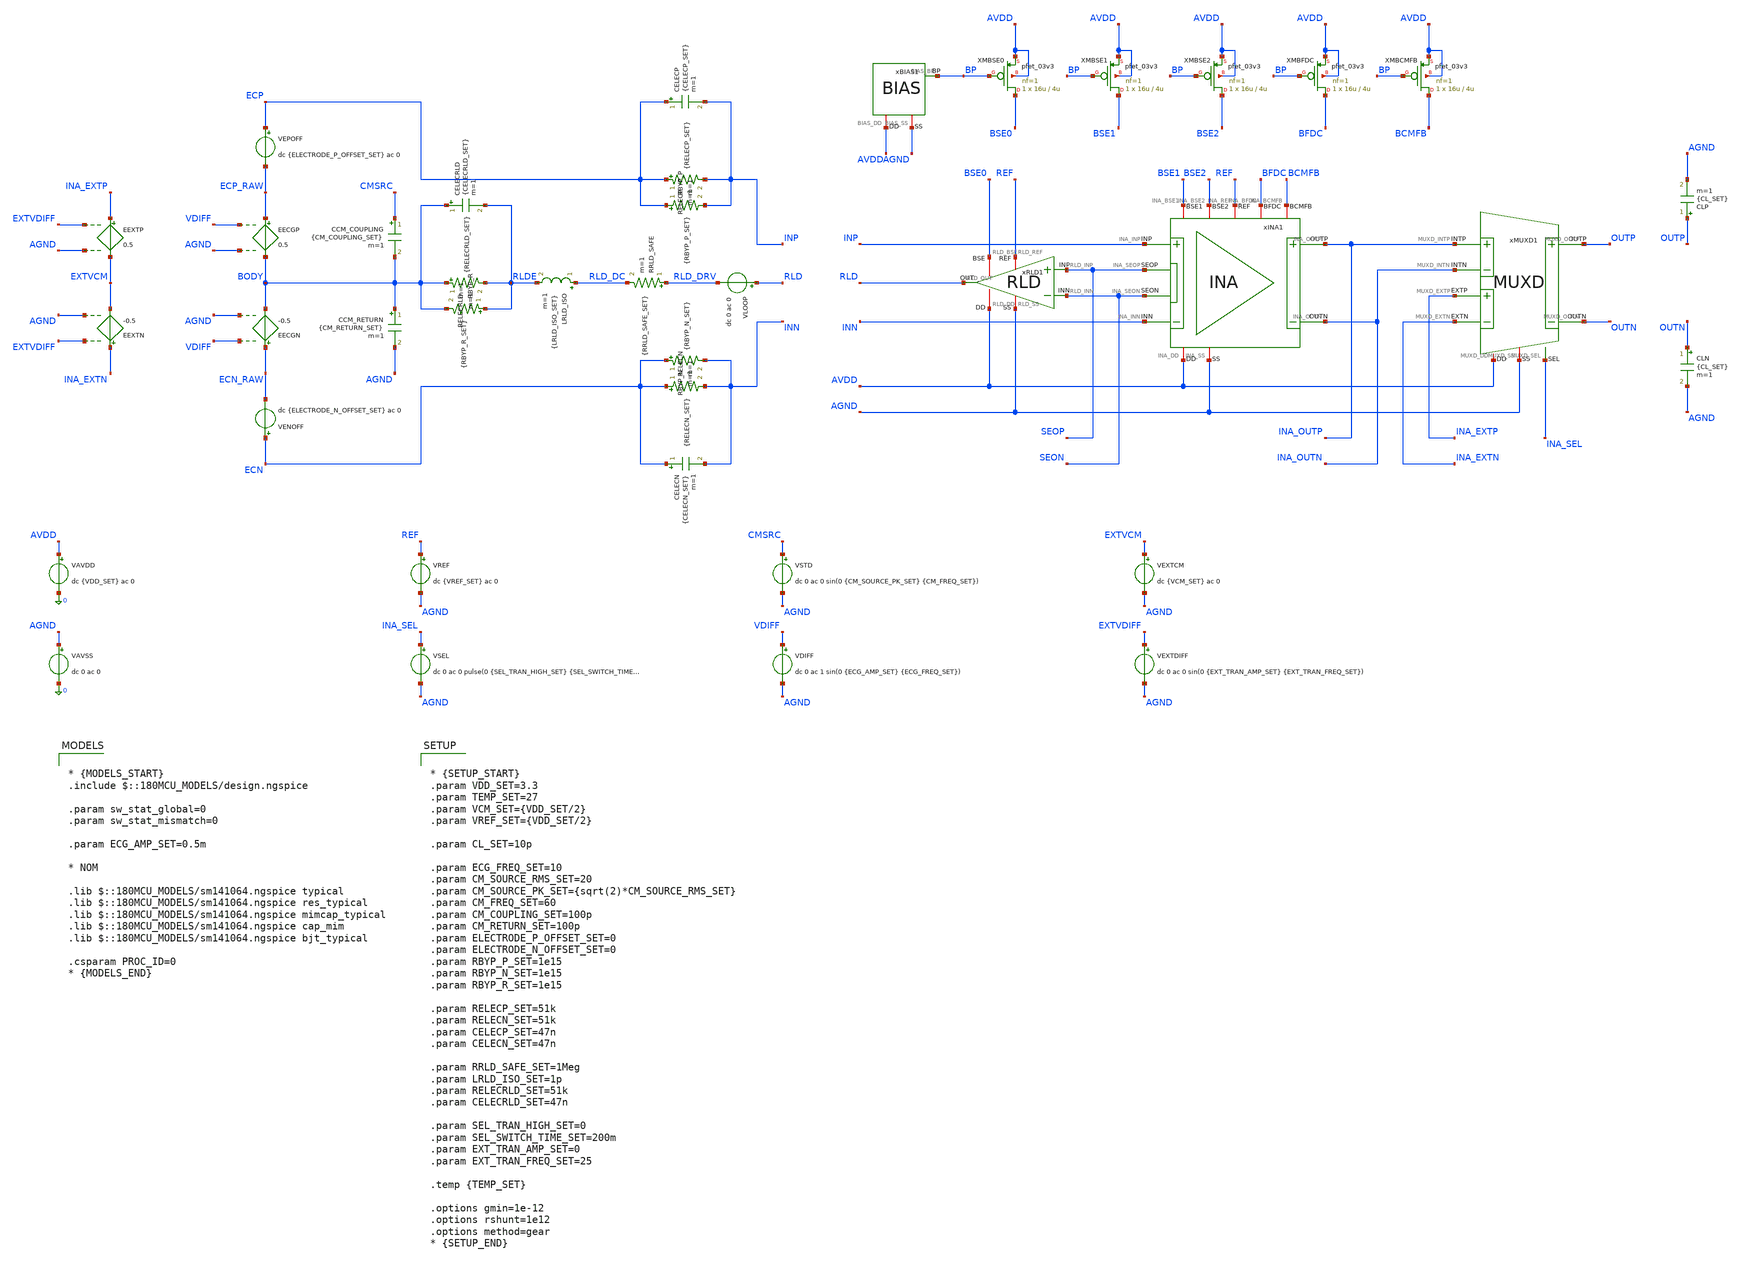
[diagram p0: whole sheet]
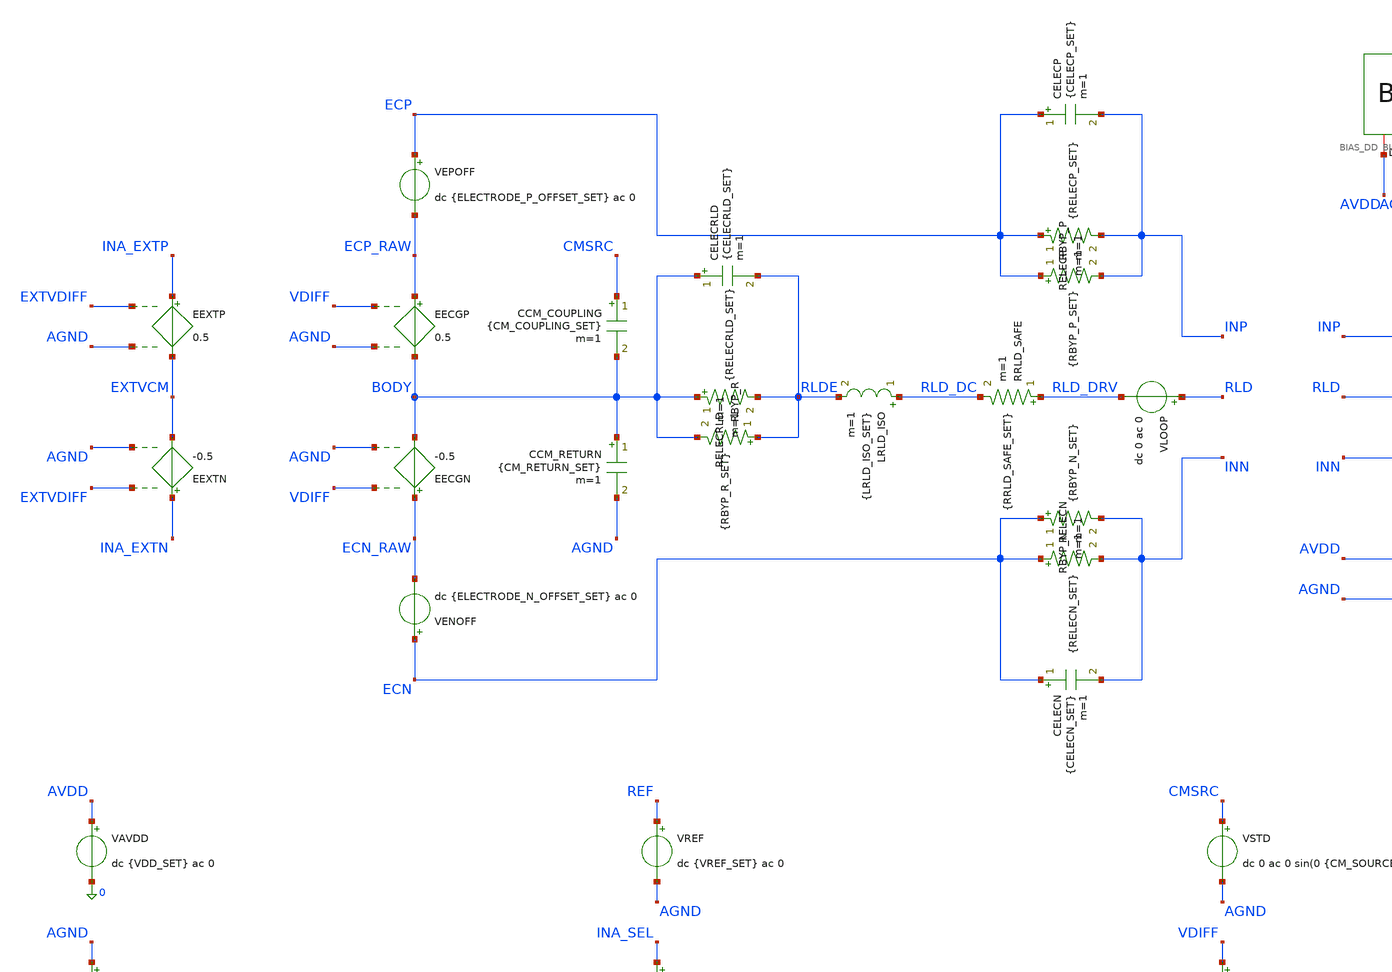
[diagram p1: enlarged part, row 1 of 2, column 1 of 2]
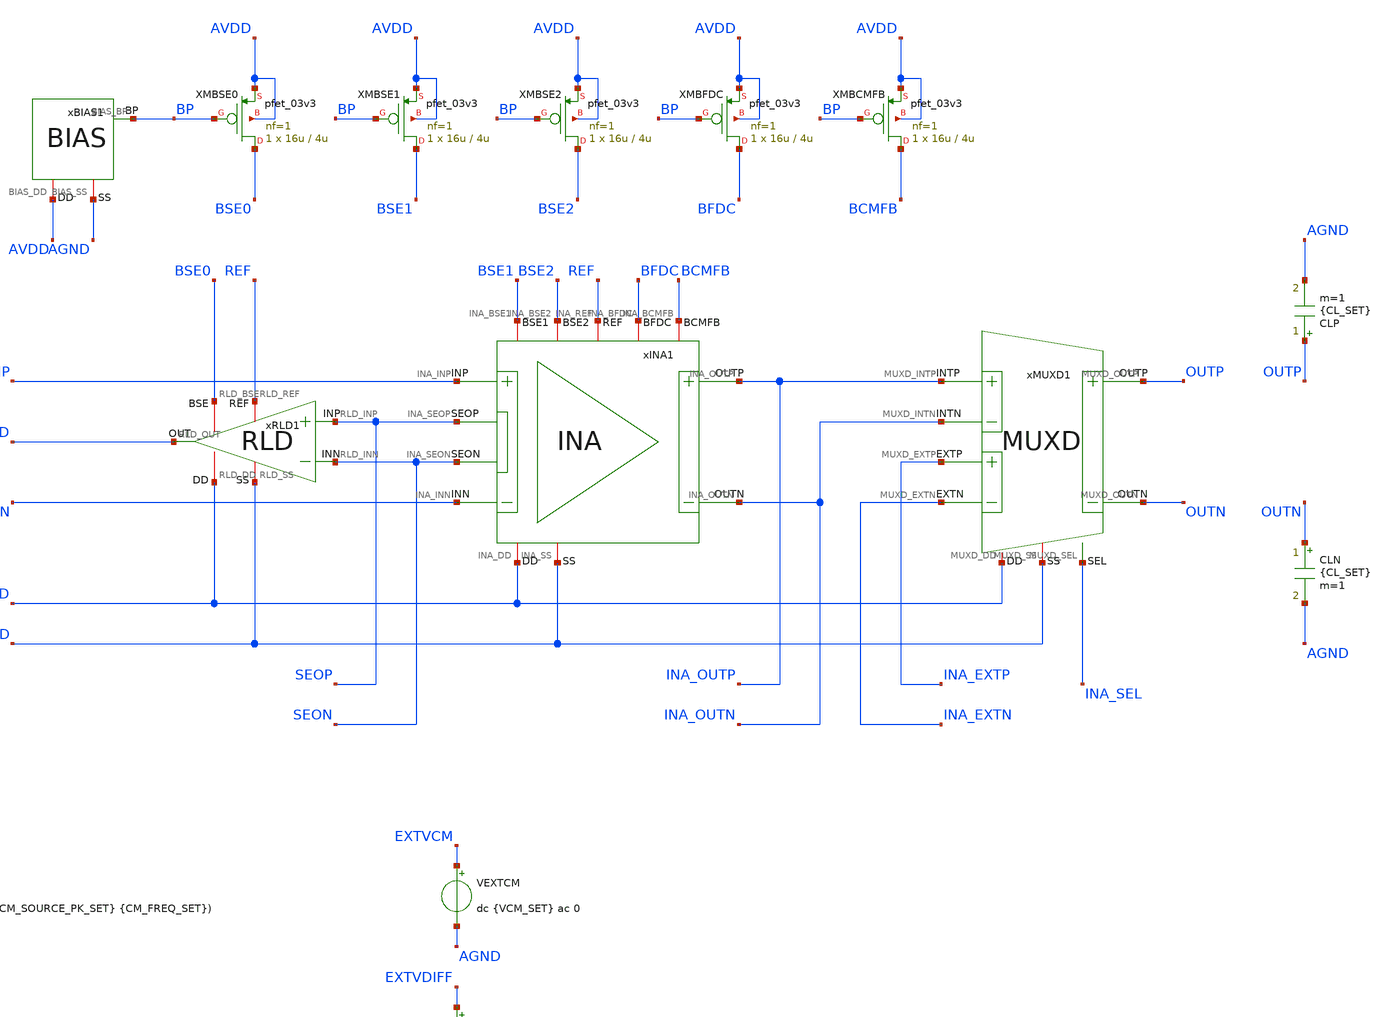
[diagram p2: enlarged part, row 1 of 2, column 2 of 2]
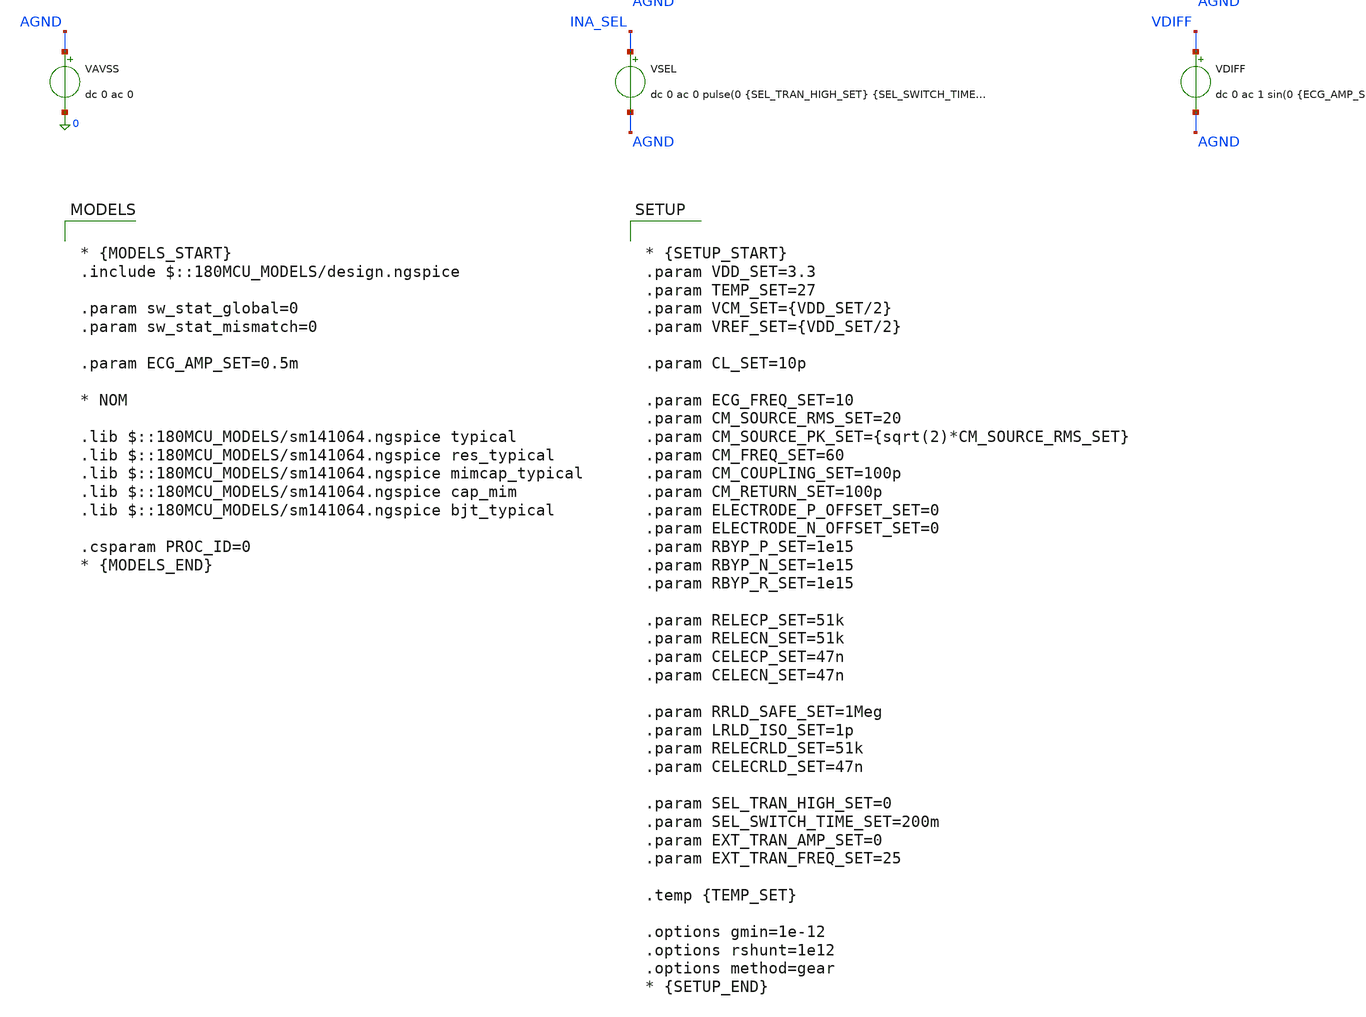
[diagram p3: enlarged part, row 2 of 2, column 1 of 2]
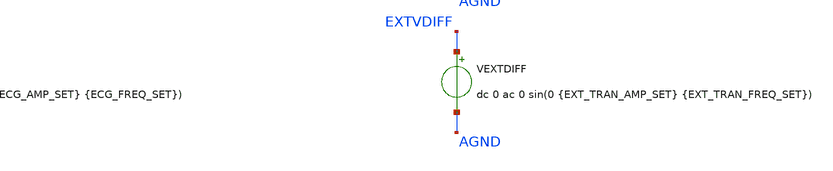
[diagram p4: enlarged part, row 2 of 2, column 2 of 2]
** sch_path: Design_Files/IC Design/Testbench/AFE_BLOCKS/INA_RLD/INA_RLD_TB_PVT_NOM.sch
**.subckt INA_RLD_TB_PVT_NOM
xMUXD1 AVDD AGND INA_OUTP INA_OUTN OUTN OUTP INA_EXTP INA_EXTN INA_SEL MUXD
xINA1 AVDD AGND INP INN INA_OUTN BFDC INA_OUTP BCMFB REF SEON SEOP BSE1 BSE2 INA
xRLD1 AVDD AGND SEOP SEON RLD REF BSE0 RLD
CLP OUTP AGND {CL_SET} m=1
CLN OUTN AGND {CL_SET} m=1
xBIAS1 AVDD AGND BP BIAS
XMBSE0 BSE0 BP AVDD AVDD pfet_03v3 L=4u W=16u nf=1 ad='int((nf+1)/2) * W/nf * 0.18u' as='int((nf+2)/2) * W/nf * 0.18u'
+ pd='2*int((nf+1)/2) * (W/nf + 0.18u)' ps='2*int((nf+2)/2) * (W/nf + 0.18u)' nrd='0.18u / W' nrs='0.18u / W'
+ sa=0 sb=0 sd=0 m=1
XMBSE1 BSE1 BP AVDD AVDD pfet_03v3 L=4u W=16u nf=1 ad='int((nf+1)/2) * W/nf * 0.18u' as='int((nf+2)/2) * W/nf * 0.18u'
+ pd='2*int((nf+1)/2) * (W/nf + 0.18u)' ps='2*int((nf+2)/2) * (W/nf + 0.18u)' nrd='0.18u / W' nrs='0.18u / W'
+ sa=0 sb=0 sd=0 m=1
XMBSE2 BSE2 BP AVDD AVDD pfet_03v3 L=4u W=16u nf=1 ad='int((nf+1)/2) * W/nf * 0.18u' as='int((nf+2)/2) * W/nf * 0.18u'
+ pd='2*int((nf+1)/2) * (W/nf + 0.18u)' ps='2*int((nf+2)/2) * (W/nf + 0.18u)' nrd='0.18u / W' nrs='0.18u / W'
+ sa=0 sb=0 sd=0 m=1
XMBFDC BFDC BP AVDD AVDD pfet_03v3 L=4u W=16u nf=1 ad='int((nf+1)/2) * W/nf * 0.18u' as='int((nf+2)/2) * W/nf * 0.18u'
+ pd='2*int((nf+1)/2) * (W/nf + 0.18u)' ps='2*int((nf+2)/2) * (W/nf + 0.18u)' nrd='0.18u / W' nrs='0.18u / W'
+ sa=0 sb=0 sd=0 m=1
XMBCMFB BCMFB BP AVDD AVDD pfet_03v3 L=4u W=16u nf=1 ad='int((nf+1)/2) * W/nf * 0.18u' as='int((nf+2)/2) * W/nf * 0.18u'
+ pd='2*int((nf+1)/2) * (W/nf + 0.18u)' ps='2*int((nf+2)/2) * (W/nf + 0.18u)' nrd='0.18u / W' nrs='0.18u / W'
+ sa=0 sb=0 sd=0 m=1
VAVDD AVDD 0 dc {VDD_SET} ac 0
.save i(vavdd)
VAVSS AGND 0 dc 0 ac 0
VSTD CMSRC AGND dc 0 ac 0 sin(0 {CM_SOURCE_PK_SET} {CM_FREQ_SET})
EECGP ECP_RAW BODY VDIFF AGND 0.5
EECGN ECN_RAW BODY VDIFF AGND -0.5
EEXTP INA_EXTP EXTVCM EXTVDIFF AGND 0.5
VDIFF VDIFF AGND dc 0 ac 1 sin(0 {ECG_AMP_SET} {ECG_FREQ_SET})
VLOOP RLD RLD_DRV dc 0 ac 0
.save i(vloop)
VSEL INA_SEL AGND dc 0 ac 0 pulse(0 {SEL_TRAN_HIGH_SET} {SEL_SWITCH_TIME_SET} 1u 1u 400m 800m)
VEXTCM EXTVCM AGND dc {VCM_SET} ac 0
VEXTDIFF EXTVDIFF AGND dc 0 ac 0 sin(0 {EXT_TRAN_AMP_SET} {EXT_TRAN_FREQ_SET})
EEXTN INA_EXTN EXTVCM EXTVDIFF AGND -0.5
CCM_COUPLING CMSRC BODY {CM_COUPLING_SET} m=1
RELECP ECP INP {RELECP_SET} m=1
RELECN ECN INN {RELECN_SET} m=1
CELECP ECP INP {CELECP_SET} m=1
CELECN ECN INN {CELECN_SET} m=1
RRLD_SAFE RLD_DRV RLD_DC {RRLD_SAFE_SET} m=1
RELECRLD BODY RLDE {RELECRLD_SET} m=1
CELECRLD BODY RLDE {CELECRLD_SET} m=1
VEPOFF ECP ECP_RAW dc {ELECTRODE_P_OFFSET_SET} ac 0
VENOFF ECN ECN_RAW dc {ELECTRODE_N_OFFSET_SET} ac 0
CCM_RETURN BODY AGND {CM_RETURN_SET} m=1
RBYP_P ECP INP {RBYP_P_SET} m=1
RBYP_N ECN INN {RBYP_N_SET} m=1
RBYP_R RLDE BODY {RBYP_R_SET} m=1
LRLD_ISO RLD_DC RLDE {LRLD_ISO_SET} m=1
VREF REF AGND dc {VREF_SET} ac 0
.save i(vref)
**** begin user architecture code

* {MODELS_START}
.include $::180MCU_MODELS/design.ngspice

.param sw_stat_global=0
.param sw_stat_mismatch=0

.param ECG_AMP_SET=0.5m

* NOM

.lib $::180MCU_MODELS/sm141064.ngspice typical
.lib $::180MCU_MODELS/sm141064.ngspice res_typical
.lib $::180MCU_MODELS/sm141064.ngspice mimcap_typical
.lib $::180MCU_MODELS/sm141064.ngspice cap_mim
.lib $::180MCU_MODELS/sm141064.ngspice bjt_typical

.csparam PROC_ID=0
* {MODELS_END}



* {SETUP_START}
.param VDD_SET=3.3
.param TEMP_SET=27
.param VCM_SET={VDD_SET/2}
.param VREF_SET={VDD_SET/2}

.param CL_SET=10p

.param ECG_FREQ_SET=10
.param CM_SOURCE_RMS_SET=20
.param CM_SOURCE_PK_SET={sqrt(2)*CM_SOURCE_RMS_SET}
.param CM_FREQ_SET=60
.param CM_COUPLING_SET=100p
.param CM_RETURN_SET=100p
.param ELECTRODE_P_OFFSET_SET=0
.param ELECTRODE_N_OFFSET_SET=0
.param RBYP_P_SET=1e15
.param RBYP_N_SET=1e15
.param RBYP_R_SET=1e15

.param RELECP_SET=51k
.param RELECN_SET=51k
.param CELECP_SET=47n
.param CELECN_SET=47n

.param RRLD_SAFE_SET=1Meg
.param LRLD_ISO_SET=1p
.param RELECRLD_SET=51k
.param CELECRLD_SET=47n

.param SEL_TRAN_HIGH_SET=0
.param SEL_SWITCH_TIME_SET=200m
.param EXT_TRAN_AMP_SET=0
.param EXT_TRAN_FREQ_SET=25

.temp {TEMP_SET}

.options gmin=1e-12
.options rshunt=1e12
.options method=gear
* {SETUP_END}




* {MEAS_START}
.control

destroy all

set noaskquit
set wr_singlescale
unset wr_vecnames

option klu
option numdgt=15
option method=gear
option maxord=2
option plotwinsize=0

if $&PROC_ID = 0
set proc=NOM
else
if $&PROC_ID = 1
set proc=FF
else
if $&PROC_ID = 2
set proc=SS
else
if $&PROC_ID = 3
set proc=FS
else
set proc=SF
end
end
end
end

shell mkdir -p /foss/designs/ECG_Acquisition_IC/Measurement_Results/IC_Simulation/AFE_BLOCKS/INA_RLD/{$proc}.Result_txt
shell rm -f /foss/designs/ECG_Acquisition_IC/Measurement_Results/IC_Simulation/AFE_BLOCKS/INA_RLD/{$proc}.Result_txt/{$proc}.*.txt

foreach vddval 3.3 3.0 3.6
foreach tval 27 -40 125

if $vddval = 3.3
if $tval = 27
set env=nom
else
if $tval = -40
set env=tl
else
set env=th
end
end
else
if $vddval = 3.0
if $tval = 27
set env=vl
else
if $tval = -40
set env=vltl
else
set env=vlth
end
end
else
if $tval = 27
set env=vh
else
if $tval = -40
set env=vhtl
else
set env=vhth
end
end
end
end

alterparam VDD_SET=$vddval
alterparam TEMP_SET=$tval

reset

save all
save @m.xmbse0.m0[id]
save @m.xmbse1.m0[id]
save @m.xmbse2.m0[id]
save @m.xmbfdc.m0[id]
save @m.xmbcmfb.m0[id]

foreach emode 0

* NOMINAL ELECTRODE MODEL
set elec=bal
alter RELECP 51k
alter RELECN 51k
alter CELECP 47n
alter CELECN 47n
alter RELECRLD 51k
alter CELECRLD 47n
alter RBYP_P 1e15
alter RBYP_N 1e15
alter RBYP_R 1e15


* OFFSET

alter RRLD_SAFE 1Meg
alter @VSEL[DC]=0
alter @VDIFF[DC]=0

alter @VDIFF[ACMAG]=0
alter @VSTD[ACMAG]=0
alter @VLOOP[ACMAG]=0
alter @VEXTDIFF[ACMAG]=0
alter @VREF[ACMAG]=0
alter @VAVDD[ACMAG]=0
alter @VAVSS[ACMAG]=0

dc VDIFF -3m 3m 50u

let ina_out_diff=v(INA_OUTP)-v(INA_OUTN)

meas dc vos_meas when ina_out_diff=0 cross=1

set vos_val=$&vos_meas

echo $vos_val > /foss/designs/ECG_Acquisition_IC/Measurement_Results/IC_Simulation/AFE_BLOCKS/INA_RLD/{$proc}.Result_txt/{$proc}.vos_{$env}_{$elec}.txt

destroy all

alter @VDIFF[DC]=$vos_val


* OP

alter RRLD_SAFE 1Meg
alter @VSEL[DC]=0

alter @VDIFF[ACMAG]=0
alter @VSTD[ACMAG]=0
alter @VLOOP[ACMAG]=0
alter @VEXTDIFF[ACMAG]=0
alter @VREF[ACMAG]=0
alter @VAVDD[ACMAG]=0
alter @VAVSS[ACMAG]=0

op

let vin_cm=0.5*(v(INP)+v(INN))-v(AGND)
let vin_diff=v(INP)-v(INN)
let se_cm=0.5*(v(SEOP)+v(SEON))-v(AGND)
let se_diff=v(SEOP)-v(SEON)
let ina_out_cm=0.5*(v(INA_OUTP)+v(INA_OUTN))-v(AGND)
let ina_out_diff=v(INA_OUTP)-v(INA_OUTN)
let out_cm=0.5*(v(OUTP)+v(OUTN))-v(AGND)
let out_diff=v(OUTP)-v(OUTN)

let idd_total=abs(vavdd#branch)
let power_total=(v(AVDD)-v(AGND))*idd_total
let irld=abs(vloop#branch)

let ibse0=abs(@m.xmbse0.m0[id])
let ibse1=abs(@m.xmbse1.m0[id])
let ibse2=abs(@m.xmbse2.m0[id])
let ibfdc=abs(@m.xmbfdc.m0[id])
let ibcmfb=abs(@m.xmbcmfb.m0[id])

wrdata /foss/designs/ECG_Acquisition_IC/Measurement_Results/IC_Simulation/AFE_BLOCKS/INA_RLD/{$proc}.Result_txt/{$proc}.op_{$env}_{$elec}.txt
+ v(AVDD) v(REF) v(BP) vin_cm vin_diff v(SEOP) v(SEON) se_cm se_diff v(INA_OUTP) v(INA_OUTN) ina_out_cm
+ ina_out_diff v(OUTP) v(OUTN) out_cm out_diff v(RLD) v(BODY) irld idd_total power_total ibse0 ibse1 ibse2
+ ibfdc ibcmfb

destroy all


* INA AC

alter RRLD_SAFE 1Meg
alter @VSEL[DC]=0

alter @VDIFF[ACMAG]=1
alter @VDIFF[ACPHASE]=0
alter @VSTD[ACMAG]=0
alter @VLOOP[ACMAG]=0
alter @VEXTDIFF[ACMAG]=0
alter @VREF[ACMAG]=0
alter @VAVDD[ACMAG]=0
alter @VAVSS[ACMAG]=0

ac dec 50 0.01 10Meg

let vin_diff=v(INP)-v(INN)
let se_diff=v(SEOP)-v(SEON)
let ina_out_diff=v(INA_OUTP)-v(INA_OUTN)
let out_diff=v(OUTP)-v(OUTN)

let vin_diff_real=real(vin_diff)
let vin_diff_imag=imag(vin_diff)

let se_diff_real=real(se_diff)
let se_diff_imag=imag(se_diff)

let ina_out_diff_real=real(ina_out_diff)
let ina_out_diff_imag=imag(ina_out_diff)

let out_diff_real=real(out_diff)
let out_diff_imag=imag(out_diff)

let rld_real=real(v(RLD))
let rld_imag=imag(v(RLD))

setscale frequency

wrdata /foss/designs/ECG_Acquisition_IC/Measurement_Results/IC_Simulation/AFE_BLOCKS/INA_RLD/{$proc}.Result_txt/{$proc}.diff_ac_{$env}_{$elec}.txt
+ vin_diff_real vin_diff_imag se_diff_real se_diff_imag ina_out_diff_real ina_out_diff_imag out_diff_real
+ out_diff_imag rld_real rld_imag

destroy all


* RLD OFF

* Keep the DC bias; isolate the RLD path in AC.
alter RRLD_SAFE 1Meg
alter LRLD_ISO 1e12
alter @VSEL[DC]=0

alter @VDIFF[ACMAG]=0
alter @VSTD[ACMAG]=1
alter @VSTD[ACPHASE]=0
alter @VLOOP[ACMAG]=0
alter @VEXTDIFF[ACMAG]=0
alter @VREF[ACMAG]=0
alter @VAVDD[ACMAG]=0
alter @VAVSS[ACMAG]=0

op

let rld_off_vin_cm=0.5*(v(INP)+v(INN))-v(AGND)
let rld_off_body=v(BODY)-v(AGND)

wrdata /foss/designs/ECG_Acquisition_IC/Measurement_Results/IC_Simulation/AFE_BLOCKS/INA_RLD/{$proc}.Result_txt/{$proc}.rld_off_op_{$env}_{$elec}.txt
+ rld_off_vin_cm rld_off_body v(INP) v(INN)

destroy all

ac dec 50 0.01 100k

let vcm_src=v(CMSRC)-v(AGND)
let body=v(BODY)-v(AGND)
let vin_cm=0.5*(v(INP)+v(INN))-v(AGND)
let se_cm=0.5*(v(SEOP)+v(SEON))-v(AGND)
let ina_out_diff=v(INA_OUTP)-v(INA_OUTN)
let out_diff=v(OUTP)-v(OUTN)

let vcm_src_real=real(vcm_src)
let vcm_src_imag=imag(vcm_src)

let body_real=real(body)
let body_imag=imag(body)

let vin_cm_real=real(vin_cm)
let vin_cm_imag=imag(vin_cm)

let se_cm_real=real(se_cm)
let se_cm_imag=imag(se_cm)

let ina_out_diff_real=real(ina_out_diff)
let ina_out_diff_imag=imag(ina_out_diff)

let out_diff_real=real(out_diff)
let out_diff_imag=imag(out_diff)

let rld_real=real(v(RLD))
let rld_imag=imag(v(RLD))

setscale frequency

wrdata /foss/designs/ECG_Acquisition_IC/Measurement_Results/IC_Simulation/AFE_BLOCKS/INA_RLD/{$proc}.Result_txt/{$proc}.cm_off_ac_{$env}_{$elec}.txt
+ vcm_src_real vcm_src_imag body_real body_imag vin_cm_real vin_cm_imag se_cm_real se_cm_imag out_diff_real
+ out_diff_imag rld_real rld_imag

wrdata /foss/designs/ECG_Acquisition_IC/Measurement_Results/IC_Simulation/AFE_BLOCKS/INA_RLD/{$proc}.Result_txt/{$proc}.ina_cmrr_ac_{$env}_{$elec}.txt
+ vin_cm_real vin_cm_imag ina_out_diff_real ina_out_diff_imag

destroy all


* RLD ON

alter RRLD_SAFE 1Meg
alter LRLD_ISO 1p
alter @VSEL[DC]=0

alter @VDIFF[ACMAG]=0
alter @VSTD[ACMAG]=1
alter @VSTD[ACPHASE]=0
alter @VLOOP[ACMAG]=0
alter @VEXTDIFF[ACMAG]=0
alter @VREF[ACMAG]=0
alter @VAVDD[ACMAG]=0
alter @VAVSS[ACMAG]=0

ac dec 50 0.01 10k

let vcm_src=v(CMSRC)-v(AGND)
let body=v(BODY)-v(AGND)
let vin_cm=0.5*(v(INP)+v(INN))-v(AGND)
let se_cm=0.5*(v(SEOP)+v(SEON))-v(AGND)
let out_diff=v(OUTP)-v(OUTN)

let vcm_src_real=real(vcm_src)
let vcm_src_imag=imag(vcm_src)

let body_real=real(body)
let body_imag=imag(body)

let vin_cm_real=real(vin_cm)
let vin_cm_imag=imag(vin_cm)

let se_cm_real=real(se_cm)
let se_cm_imag=imag(se_cm)

let out_diff_real=real(out_diff)
let out_diff_imag=imag(out_diff)

let rld_real=real(v(RLD))
let rld_imag=imag(v(RLD))

setscale frequency

wrdata /foss/designs/ECG_Acquisition_IC/Measurement_Results/IC_Simulation/AFE_BLOCKS/INA_RLD/{$proc}.Result_txt/{$proc}.cm_on_ac_{$env}_{$elec}.txt
+ vcm_src_real vcm_src_imag body_real body_imag vin_cm_real vin_cm_imag se_cm_real se_cm_imag out_diff_real
+ out_diff_imag rld_real rld_imag

destroy all


* PSRR+

alter RRLD_SAFE 1Meg
alter @VSEL[DC]=0

alter @VDIFF[ACMAG]=0
alter @VSTD[ACMAG]=0
alter @VLOOP[ACMAG]=0
alter @VEXTDIFF[ACMAG]=0
alter @VREF[ACMAG]=0

alter @VAVDD[ACMAG]=1
alter @VAVDD[ACPHASE]=0
alter @VAVSS[ACMAG]=0

ac dec 50 0.01 100k

let vsup=v(AVDD)-v(AGND)
let ina_out_diff=v(INA_OUTP)-v(INA_OUTN)
let out_diff=v(OUTP)-v(OUTN)

let vsup_real=real(vsup)
let vsup_imag=imag(vsup)

let ina_out_diff_real=real(ina_out_diff)
let ina_out_diff_imag=imag(ina_out_diff)

let out_diff_real=real(out_diff)
let out_diff_imag=imag(out_diff)

setscale frequency

wrdata /foss/designs/ECG_Acquisition_IC/Measurement_Results/IC_Simulation/AFE_BLOCKS/INA_RLD/{$proc}.Result_txt/{$proc}.psrrp_ac_{$env}_{$elec}.txt
+ vsup_real vsup_imag ina_out_diff_real ina_out_diff_imag out_diff_real out_diff_imag

destroy all


* PSRR-

alter RRLD_SAFE 1Meg
alter @VSEL[DC]=0

alter @VDIFF[ACMAG]=0
alter @VSTD[ACMAG]=0
alter @VLOOP[ACMAG]=0
alter @VEXTDIFF[ACMAG]=0
alter @VREF[ACMAG]=0

alter @VAVDD[ACMAG]=0
alter @VAVSS[ACMAG]=1
alter @VAVSS[ACPHASE]=0

ac dec 50 0.01 100k

let vsup=v(AVDD)-v(AGND)
let ina_out_diff=v(INA_OUTP)-v(INA_OUTN)
let out_diff=v(OUTP)-v(OUTN)

let vsup_real=real(vsup)
let vsup_imag=imag(vsup)

let ina_out_diff_real=real(ina_out_diff)
let ina_out_diff_imag=imag(ina_out_diff)

let out_diff_real=real(out_diff)
let out_diff_imag=imag(out_diff)

setscale frequency

wrdata /foss/designs/ECG_Acquisition_IC/Measurement_Results/IC_Simulation/AFE_BLOCKS/INA_RLD/{$proc}.Result_txt/{$proc}.psrrn_ac_{$env}_{$elec}.txt
+ vsup_real vsup_imag ina_out_diff_real ina_out_diff_imag out_diff_real out_diff_imag

destroy all


* RLD LOOP

alter RRLD_SAFE 1Meg
alter LRLD_ISO 1p
alter @VSEL[DC]=0

alter @VDIFF[ACMAG]=0
alter @VSTD[ACMAG]=0
alter @VLOOP[ACMAG]=1
alter @VLOOP[ACPHASE]=0
alter @VEXTDIFF[ACMAG]=0
alter @VREF[ACMAG]=0
alter @VAVDD[ACMAG]=0
alter @VAVSS[ACMAG]=0

ac dec 50 0.01 100k

let loop_in=v(RLD_DRV)-v(AGND)
let loop_out=v(RLD)-v(AGND)
let body=v(BODY)-v(AGND)
let vin_cm=0.5*(v(INP)+v(INN))-v(AGND)
let se_cm=0.5*(v(SEOP)+v(SEON))-v(AGND)

let loop_in_real=real(loop_in)
let loop_in_imag=imag(loop_in)

let loop_out_real=real(loop_out)
let loop_out_imag=imag(loop_out)

let body_real=real(body)
let body_imag=imag(body)

let vin_cm_real=real(vin_cm)
let vin_cm_imag=imag(vin_cm)

let se_cm_real=real(se_cm)
let se_cm_imag=imag(se_cm)

setscale frequency

wrdata /foss/designs/ECG_Acquisition_IC/Measurement_Results/IC_Simulation/AFE_BLOCKS/INA_RLD/{$proc}.Result_txt/{$proc}.rld_loop_ac_{$env}_{$elec}.txt
+ loop_in_real loop_in_imag loop_out_real loop_out_imag body_real body_imag vin_cm_real vin_cm_imag se_cm_real
+ se_cm_imag

destroy all


* NOISE

alter RRLD_SAFE 1Meg
alter @VSEL[DC]=0

alter @VDIFF[ACMAG]=1
alter @VDIFF[ACPHASE]=0
alter @VSTD[ACMAG]=0
alter @VLOOP[ACMAG]=0
alter @VEXTDIFF[ACMAG]=0
alter @VREF[ACMAG]=0
alter @VAVDD[ACMAG]=0
alter @VAVSS[ACMAG]=0

option sparse

noise v(OUTP,OUTN) VDIFF dec 50 0.05 500

setplot previous
setscale frequency

wrdata /foss/designs/ECG_Acquisition_IC/Measurement_Results/IC_Simulation/AFE_BLOCKS/INA_RLD/{$proc}.Result_txt/{$proc}.noise_{$env}_{$elec}.txt
+ onoise_spectrum inoise_spectrum

destroy all


* INA VTC

* Balanced electrodes, RLD ON, internal INA path.
alter RELECP 51k
alter RELECN 51k
alter CELECP 47n
alter CELECN 47n
alter RELECRLD 51k
alter CELECRLD 47n
alter RBYP_P 1e15
alter RBYP_N 1e15
alter RBYP_R 1e15
alter RRLD_SAFE 1Meg
alter LRLD_ISO 1p
alter @VSEL[DC]=0

* No AC excitation.
alter @VDIFF[ACMAG]=0
alter @VSTD[ACMAG]=0
alter @VLOOP[ACMAG]=0
alter @VEXTDIFF[ACMAG]=0
alter @VREF[ACMAG]=0
alter @VAVDD[ACMAG]=0
alter @VAVSS[ACMAG]=0

* Sweep beyond the required ECG plus offset range.
dc VDIFF -20m 20m 50u

let vin_diff=v(INP)-v(INN)
let ina_outp=v(INA_OUTP)-v(AGND)
let ina_outn=v(INA_OUTN)-v(AGND)
let ina_out_cm=0.5*(v(INA_OUTP)+v(INA_OUTN))-v(AGND)
let ina_out_diff=v(INA_OUTP)-v(INA_OUTN)

wrdata /foss/designs/ECG_Acquisition_IC/Measurement_Results/IC_Simulation/AFE_BLOCKS/INA_RLD/{$proc}.Result_txt/{$proc}.vtc_{$env}_{$elec}.txt
+ vin_diff ina_outp ina_outn ina_out_cm ina_out_diff

destroy all


* THD AT 60 HZ

* 5 mVpp (2.5 mV peak) differential input at 60 Hz.
alterparam ECG_AMP_SET=2.5m
alterparam ECG_FREQ_SET=60
alterparam CM_SOURCE_RMS_SET=0
alterparam ELECTRODE_P_OFFSET_SET=0
alterparam ELECTRODE_N_OFFSET_SET=0

reset

save v(INP) v(INN)
save v(INA_OUTP) v(INA_OUTN)
save v(OUTP) v(OUTN)

* Balanced electrodes, RLD ON, internal INA path.
alter RELECP 51k
alter RELECN 51k
alter CELECP 47n
alter CELECN 47n
alter RELECRLD 51k
alter CELECRLD 47n
alter RBYP_P 1e15
alter RBYP_N 1e15
alter RBYP_R 1e15
alter RRLD_SAFE 1Meg
alter LRLD_ISO 1p
alter @VSEL[DC]=0
alter @VDIFF[DC]=0

* 100 ms settling and 10 measured cycles.
tran 50u 266.666667m 100m

let vin_diff=v(INP)-v(INN)
let ina_out_diff=v(INA_OUTP)-v(INA_OUTN)
let out_diff=v(OUTP)-v(OUTN)

wrdata /foss/designs/ECG_Acquisition_IC/Measurement_Results/IC_Simulation/AFE_BLOCKS/INA_RLD/{$proc}.Result_txt/{$proc}.thd_60_{$env}_{$elec}.txt
+ vin_diff ina_out_diff out_diff

destroy all


* Restore normal PVT stimulus.
alterparam ECG_AMP_SET=0.5m
alterparam ECG_FREQ_SET=10
alterparam CM_SOURCE_RMS_SET=20


end

end
end


* STD CMR - ACTIVE LEADS (FULL 3 x 3 VDD/TEMP MATRIX)

foreach rti_vdd 3.3 3.0 3.6
foreach rti_temp 27 -40 125

if $rti_vdd = 3.3
if $rti_temp = 27
set env=nom
else
if $rti_temp = -40
set env=tl
else
set env=th
end
end
else
if $rti_vdd = 3.0
if $rti_temp = 27
set env=vl
else
if $rti_temp = -40
set env=vltl
else
set env=vlth
end
end
else
if $rti_temp = 27
set env=vh
else
if $rti_temp = -40
set env=vhtl
else
set env=vhth
end
end
end
end

alterparam VDD_SET=$rti_vdd
alterparam TEMP_SET=$rti_temp
alterparam ECG_AMP_SET=0
alterparam CM_SOURCE_RMS_SET=20
alterparam CM_FREQ_SET=60
alterparam ELECTRODE_P_OFFSET_SET=0
alterparam ELECTRODE_N_OFFSET_SET=0

reset
save all

alter RRLD_SAFE 1Meg
alter LRLD_ISO 1p
alter @VSEL[DC]=0
alter RELECP 51k
alter CELECP 47n
alter RELECN 51k
alter CELECN 47n
alter RELECRLD 51k
alter CELECRLD 47n
alter RBYP_P 1e15
alter RBYP_N 1e15
alter RBYP_R 1e15

* BAL

tran 200u 500m

let vin_cm=0.5*(v(INP)+v(INN))-v(AGND)
let vin_diff=v(INP)-v(INN)
let out_diff=v(OUTP)-v(OUTN)

wrdata /foss/designs/ECG_Acquisition_IC/Measurement_Results/IC_Simulation/AFE_BLOCKS/INA_RLD/{$proc}.Result_txt/{$proc}.std_bal_{$env}.txt
+ v(CMSRC) v(BODY) vin_cm vin_diff out_diff v(RLD)

destroy all

* MIS-P

alter RBYP_P 1
alter RBYP_N 1e15
alter RBYP_R 1e15

tran 200u 500m

let vin_cm=0.5*(v(INP)+v(INN))-v(AGND)
let vin_diff=v(INP)-v(INN)
let out_diff=v(OUTP)-v(OUTN)

wrdata /foss/designs/ECG_Acquisition_IC/Measurement_Results/IC_Simulation/AFE_BLOCKS/INA_RLD/{$proc}.Result_txt/{$proc}.std_misp_{$env}.txt
+ v(CMSRC) v(BODY) vin_cm vin_diff out_diff v(RLD)

destroy all

* MIS-N

alter RBYP_P 1e15
alter RBYP_N 1
alter RBYP_R 1e15

tran 200u 500m

let vin_cm=0.5*(v(INP)+v(INN))-v(AGND)
let vin_diff=v(INP)-v(INN)
let out_diff=v(OUTP)-v(OUTN)

wrdata /foss/designs/ECG_Acquisition_IC/Measurement_Results/IC_Simulation/AFE_BLOCKS/INA_RLD/{$proc}.Result_txt/{$proc}.std_misn_{$env}.txt
+ v(CMSRC) v(BODY) vin_cm vin_diff out_diff v(RLD)

destroy all

* MIS-RLD

alter RBYP_P 1e15
alter RBYP_N 1e15
alter RBYP_R 1

tran 200u 500m

let vin_cm=0.5*(v(INP)+v(INN))-v(AGND)
let vin_diff=v(INP)-v(INN)
let out_diff=v(OUTP)-v(OUTN)

wrdata /foss/designs/ECG_Acquisition_IC/Measurement_Results/IC_Simulation/AFE_BLOCKS/INA_RLD/{$proc}.Result_txt/{$proc}.std_misrld_{$env}.txt
+ v(CMSRC) v(BODY) vin_cm vin_diff out_diff v(RLD)

destroy all

end
end


* SEL NOM

if $&PROC_ID = 0

alterparam VDD_SET=3.3
alterparam TEMP_SET=27
alterparam ECG_AMP_SET=0.5m
alterparam CM_SOURCE_RMS_SET=0
alterparam ELECTRODE_P_OFFSET_SET=0
alterparam ELECTRODE_N_OFFSET_SET=0
alterparam SEL_TRAN_HIGH_SET=3.3
alterparam EXT_TRAN_AMP_SET=50m
alterparam EXT_TRAN_FREQ_SET=25

reset
save all

alter RELECP 51k
alter RELECN 51k
alter CELECP 47n
alter CELECN 47n
alter RELECRLD 51k
alter CELECRLD 47n
alter RRLD_SAFE 1Meg

alter @VDIFF[DC]=0
alter @VDIFF[ACMAG]=0
alter @VSTD[ACMAG]=0
alter @VLOOP[ACMAG]=0
alter @VEXTDIFF[ACMAG]=0
alter @VREF[ACMAG]=0
alter @VAVDD[ACMAG]=0
alter @VAVSS[ACMAG]=0

tran 50u 400m

let int_in_diff=v(INP)-v(INN)
let ext_in_diff=v(INA_EXTP)-v(INA_EXTN)
let out_diff=v(OUTP)-v(OUTN)

wrdata /foss/designs/ECG_Acquisition_IC/Measurement_Results/IC_Simulation/AFE_BLOCKS/INA_RLD/{$proc}.Result_txt/{$proc}.sel_tran_nom.txt
+ v(INA_SEL) int_in_diff ext_in_diff out_diff

destroy all

end

quit

.endc
* {MEAS_END}


**** end user architecture code
**.ends
.end
